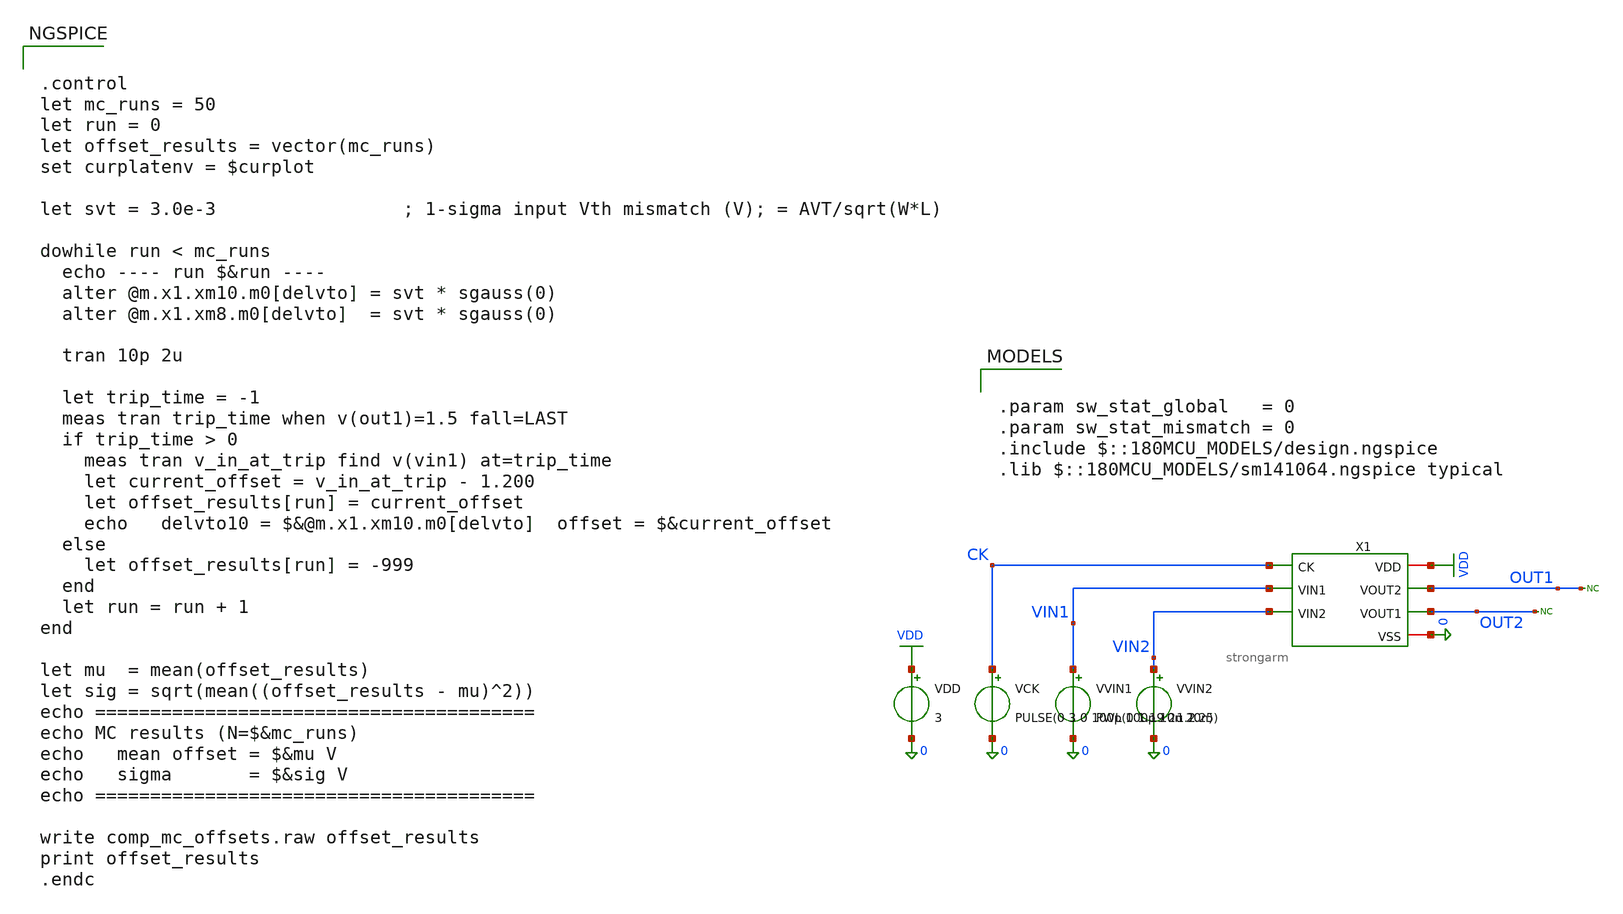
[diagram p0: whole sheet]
** sch_path: comparator/schematic/strongarm_mc_tb.sch
**.subckt strongarm_mc_tb
X1 VDD CK OUT1 OUT2 VIN1 VIN2 0 strongarm
VVIN2 VIN2 0 1.2
VVIN1 VIN1 0 PWL(0 1.19 2u 1.25)
VDD VDD 0 3
VCK CK 0 PULSE(0 3 0 100p 100p 10n 20n)
* noconn OUT2
* noconn OUT1
**** begin user architecture code

.param sw_stat_global   = 0
.param sw_stat_mismatch = 0
.include $::180MCU_MODELS/design.ngspice
.lib $::180MCU_MODELS/sm141064.ngspice typical



.control
let mc_runs = 50
let run = 0
let offset_results = vector(mc_runs)
set curplatenv = $curplot

let svt = 3.0e-3                 ; 1-sigma input Vth mismatch (V); = AVT/sqrt(W*L)

dowhile run < mc_runs
  echo ---- run $&run ----
  alter @m.x1.xm10.m0[delvto] = svt * sgauss(0)
  alter @m.x1.xm8.m0[delvto]  = svt * sgauss(0)

  tran 10p 2u

  let trip_time = -1
  meas tran trip_time when v(out1)=1.5 fall=LAST
  if trip_time > 0
    meas tran v_in_at_trip find v(vin1) at=trip_time
    let current_offset = v_in_at_trip - 1.200
    let offset_results[run] = current_offset
    echo   delvto10 = $&@m.x1.xm10.m0[delvto]  offset = $&current_offset
  else
    let offset_results[run] = -999
  end
  let run = run + 1
end

let mu  = mean(offset_results)
let sig = sqrt(mean((offset_results - mu)^2))
echo ========================================
echo MC results (N=$&mc_runs)
echo   mean offset = $&mu V
echo   sigma       = $&sig V
echo ========================================

write comp_mc_offsets.raw offset_results
print offset_results
.endc


**** end user architecture code
**.ends

* expanding   symbol:  comparator/schematic/strongarm.sym # of pins=7
** sym_path: comparator/schematic/strongarm.sym
** sch_path: comparator/schematic/strongarm.sch
.subckt strongarm VDD CK VOUT2 VOUT1 VIN1 VIN2 VSS
*.opin VOUT1
*.opin VOUT2
*.ipin VIN1
*.ipin VIN2
*.ipin CK
*.iopin VDD
*.iopin VSS
XM1 VOUT2 VOUT1 net1 net1 nfet_03v3 L=0.28u W=0.22u nf=1 ad='int((nf+1)/2) * W/nf * 0.18u' as='int((nf+2)/2) * W/nf * 0.18u'
+ pd='2*int((nf+1)/2) * (W/nf + 0.18u)' ps='2*int((nf+2)/2) * (W/nf + 0.18u)' nrd='0.18u / W' nrs='0.18u / W'
+ sa=0 sb=0 sd=0 m=1
XM2 VOUT1 VOUT2 VDD VDD pfet_03v3 L=0.28u W=0.22u nf=1 ad='int((nf+1)/2) * W/nf * 0.18u' as='int((nf+2)/2) * W/nf * 0.18u'
+ pd='2*int((nf+1)/2) * (W/nf + 0.18u)' ps='2*int((nf+2)/2) * (W/nf + 0.18u)' nrd='0.18u / W' nrs='0.18u / W'
+ sa=0 sb=0 sd=0 m=1
XM3 VOUT1 CK VDD VDD pfet_03v3 L=0.28u W=0.22u nf=1 ad='int((nf+1)/2) * W/nf * 0.18u' as='int((nf+2)/2) * W/nf * 0.18u'
+ pd='2*int((nf+1)/2) * (W/nf + 0.18u)' ps='2*int((nf+2)/2) * (W/nf + 0.18u)' nrd='0.18u / W' nrs='0.18u / W'
+ sa=0 sb=0 sd=0 m=1
XM4 net3 CK VDD VDD pfet_03v3 L=0.28u W=0.22u nf=1 ad='int((nf+1)/2) * W/nf * 0.18u' as='int((nf+2)/2) * W/nf * 0.18u'
+ pd='2*int((nf+1)/2) * (W/nf + 0.18u)' ps='2*int((nf+2)/2) * (W/nf + 0.18u)' nrd='0.18u / W' nrs='0.18u / W'
+ sa=0 sb=0 sd=0 m=1
XM5 net1 CK VDD VDD pfet_03v3 L=0.28u W=0.22u nf=1 ad='int((nf+1)/2) * W/nf * 0.18u' as='int((nf+2)/2) * W/nf * 0.18u'
+ pd='2*int((nf+1)/2) * (W/nf + 0.18u)' ps='2*int((nf+2)/2) * (W/nf + 0.18u)' nrd='0.18u / W' nrs='0.18u / W'
+ sa=0 sb=0 sd=0 m=1
XM6 VOUT2 CK VDD VDD pfet_03v3 L=0.28u W=0.22u nf=1 ad='int((nf+1)/2) * W/nf * 0.18u' as='int((nf+2)/2) * W/nf * 0.18u'
+ pd='2*int((nf+1)/2) * (W/nf + 0.18u)' ps='2*int((nf+2)/2) * (W/nf + 0.18u)' nrd='0.18u / W' nrs='0.18u / W'
+ sa=0 sb=0 sd=0 m=1
XM7 VOUT2 VOUT1 VDD VDD pfet_03v3 L=0.28u W=0.22u nf=1 ad='int((nf+1)/2) * W/nf * 0.18u' as='int((nf+2)/2) * W/nf * 0.18u'
+ pd='2*int((nf+1)/2) * (W/nf + 0.18u)' ps='2*int((nf+2)/2) * (W/nf + 0.18u)' nrd='0.18u / W' nrs='0.18u / W'
+ sa=0 sb=0 sd=0 m=1
XM8 net1 VIN2 net2 net2 nfet_03v3 L=0.28u W=0.22u nf=1 ad='int((nf+1)/2) * W/nf * 0.18u' as='int((nf+2)/2) * W/nf * 0.18u'
+ pd='2*int((nf+1)/2) * (W/nf + 0.18u)' ps='2*int((nf+2)/2) * (W/nf + 0.18u)' nrd='0.18u / W' nrs='0.18u / W'
+ sa=0 sb=0 sd=0 m=1
XM9 VOUT1 VOUT2 net3 net3 nfet_03v3 L=0.28u W=0.22u nf=1 ad='int((nf+1)/2) * W/nf * 0.18u' as='int((nf+2)/2) * W/nf * 0.18u'
+ pd='2*int((nf+1)/2) * (W/nf + 0.18u)' ps='2*int((nf+2)/2) * (W/nf + 0.18u)' nrd='0.18u / W' nrs='0.18u / W'
+ sa=0 sb=0 sd=0 m=1
XM10 net3 VIN1 net2 net2 nfet_03v3 L=0.28u W=0.22u nf=1 ad='int((nf+1)/2) * W/nf * 0.18u' as='int((nf+2)/2) * W/nf * 0.18u'
+ pd='2*int((nf+1)/2) * (W/nf + 0.18u)' ps='2*int((nf+2)/2) * (W/nf + 0.18u)' nrd='0.18u / W' nrs='0.18u / W'
+ sa=0 sb=0 sd=0 m=1
XM11 net2 CK VSS net2 nfet_03v3 L=0.28u W=0.22u nf=1 ad='int((nf+1)/2) * W/nf * 0.18u' as='int((nf+2)/2) * W/nf * 0.18u'
+ pd='2*int((nf+1)/2) * (W/nf + 0.18u)' ps='2*int((nf+2)/2) * (W/nf + 0.18u)' nrd='0.18u / W' nrs='0.18u / W'
+ sa=0 sb=0 sd=0 m=1
.ends

.GLOBAL VDD
.end
